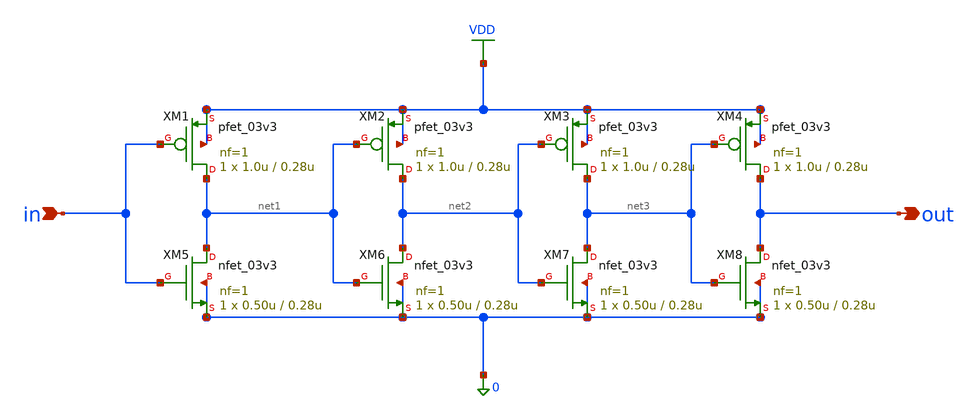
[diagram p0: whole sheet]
** sch_path: xschem/sar_adc/blocks/async_sar/delay_line.sch
**.subckt delay_line in out
*.ipin in
*.opin out
XM1 net1 in VDD VDD pfet_03v3 L=0.28u W=1.0u nf=1 ad='int((nf+1)/2) * W/nf * 0.18u' as='int((nf+2)/2) * W/nf * 0.18u'
+ pd='2*int((nf+1)/2) * (W/nf + 0.18u)' ps='2*int((nf+2)/2) * (W/nf + 0.18u)' nrd='0.18u / W' nrs='0.18u / W'
+ sa=0 sb=0 sd=0 m=1
XM5 net1 in 0 0 nfet_03v3 L=0.28u W=0.50u nf=1 ad='int((nf+1)/2) * W/nf * 0.18u' as='int((nf+2)/2) * W/nf * 0.18u'
+ pd='2*int((nf+1)/2) * (W/nf + 0.18u)' ps='2*int((nf+2)/2) * (W/nf + 0.18u)' nrd='0.18u / W' nrs='0.18u / W'
+ sa=0 sb=0 sd=0 m=1
XM2 net2 net1 VDD VDD pfet_03v3 L=0.28u W=1.0u nf=1 ad='int((nf+1)/2) * W/nf * 0.18u' as='int((nf+2)/2) * W/nf * 0.18u'
+ pd='2*int((nf+1)/2) * (W/nf + 0.18u)' ps='2*int((nf+2)/2) * (W/nf + 0.18u)' nrd='0.18u / W' nrs='0.18u / W'
+ sa=0 sb=0 sd=0 m=1
XM3 net3 net2 VDD VDD pfet_03v3 L=0.28u W=1.0u nf=1 ad='int((nf+1)/2) * W/nf * 0.18u' as='int((nf+2)/2) * W/nf * 0.18u'
+ pd='2*int((nf+1)/2) * (W/nf + 0.18u)' ps='2*int((nf+2)/2) * (W/nf + 0.18u)' nrd='0.18u / W' nrs='0.18u / W'
+ sa=0 sb=0 sd=0 m=1
XM4 out net3 VDD VDD pfet_03v3 L=0.28u W=1.0u nf=1 ad='int((nf+1)/2) * W/nf * 0.18u' as='int((nf+2)/2) * W/nf * 0.18u'
+ pd='2*int((nf+1)/2) * (W/nf + 0.18u)' ps='2*int((nf+2)/2) * (W/nf + 0.18u)' nrd='0.18u / W' nrs='0.18u / W'
+ sa=0 sb=0 sd=0 m=1
XM6 net2 net1 0 0 nfet_03v3 L=0.28u W=0.50u nf=1 ad='int((nf+1)/2) * W/nf * 0.18u' as='int((nf+2)/2) * W/nf * 0.18u'
+ pd='2*int((nf+1)/2) * (W/nf + 0.18u)' ps='2*int((nf+2)/2) * (W/nf + 0.18u)' nrd='0.18u / W' nrs='0.18u / W'
+ sa=0 sb=0 sd=0 m=1
XM7 net3 net2 0 0 nfet_03v3 L=0.28u W=0.50u nf=1 ad='int((nf+1)/2) * W/nf * 0.18u' as='int((nf+2)/2) * W/nf * 0.18u'
+ pd='2*int((nf+1)/2) * (W/nf + 0.18u)' ps='2*int((nf+2)/2) * (W/nf + 0.18u)' nrd='0.18u / W' nrs='0.18u / W'
+ sa=0 sb=0 sd=0 m=1
XM8 out net3 0 0 nfet_03v3 L=0.28u W=0.50u nf=1 ad='int((nf+1)/2) * W/nf * 0.18u' as='int((nf+2)/2) * W/nf * 0.18u'
+ pd='2*int((nf+1)/2) * (W/nf + 0.18u)' ps='2*int((nf+2)/2) * (W/nf + 0.18u)' nrd='0.18u / W' nrs='0.18u / W'
+ sa=0 sb=0 sd=0 m=1
**.ends
.GLOBAL VDD
.end
